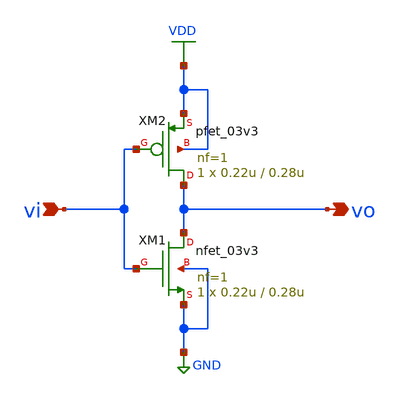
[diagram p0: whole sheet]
** sch_path: designs/inv/inv.sch
**.subckt inv vi vo
*.ipin vi
*.opin vo
XM1 vo vi GND GND nfet_03v3 L=0.28u W=0.22u nf=1 ad='int((nf+1)/2) * W/nf * 0.18u' as='int((nf+2)/2) * W/nf * 0.18u'
+ pd='2*int((nf+1)/2) * (W/nf + 0.18u)' ps='2*int((nf+2)/2) * (W/nf + 0.18u)' nrd='0.18u / W' nrs='0.18u / W'
+ sa=0 sb=0 sd=0 m=1
XM2 vo vi VDD VDD pfet_03v3 L=0.28u W=0.22u nf=1 ad='int((nf+1)/2) * W/nf * 0.18u' as='int((nf+2)/2) * W/nf * 0.18u'
+ pd='2*int((nf+1)/2) * (W/nf + 0.18u)' ps='2*int((nf+2)/2) * (W/nf + 0.18u)' nrd='0.18u / W' nrs='0.18u / W'
+ sa=0 sb=0 sd=0 m=1
**.ends
.GLOBAL VDD
.GLOBAL GND
.end
